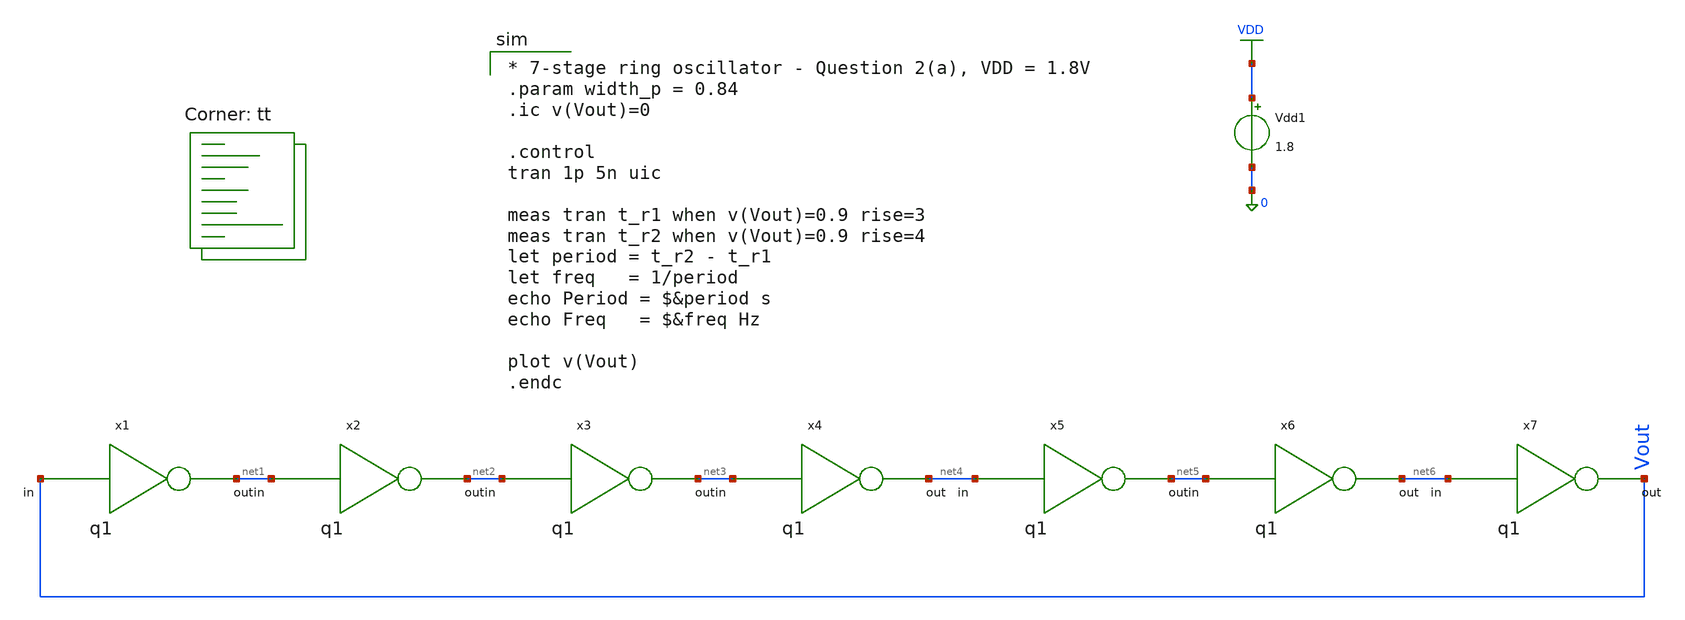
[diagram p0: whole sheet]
** sch_path: tutorial-3/source/q2a.sch
**.subckt q2a
x1 net1 Vout q1
x2 net2 net1 q1
x3 net3 net2 q1
x4 net4 net3 q1
x5 net5 net4 q1
x6 net6 net5 q1
x7 Vout net6 q1
Vdd1 VDD 0 1.8
**** begin user architecture code

* 7-stage ring oscillator - Question 2(a), VDD = 1.8V
.param width_p = 0.84
.ic v(Vout)=0

.control
tran 1p 5n uic

meas tran t_r1 when v(Vout)=0.9 rise=3
meas tran t_r2 when v(Vout)=0.9 rise=4
let period = t_r2 - t_r1
let freq   = 1/period
echo Period = $&period s
echo Freq   = $&freq Hz

plot v(Vout)
.endc

.lib $::SKYWATER_MODELS/sky130.lib.spice tt
**** end user architecture code
**.ends

* expanding   symbol:  q1.sym # of pins=2
** sym_path: tutorial-3/source/q1.sym
** sch_path: tutorial-3/source/q1.sch
.subckt q1 out in
*.ipin in
*.opin out
XM1 out in VDD VDD sky130_fd_pr__pfet_01v8 L=0.15 W={width_p} nf=1 ad='int((nf+1)/2) * W/nf * 0.29' as='int((nf+2)/2) * W/nf * 0.29'
+ pd='2*int((nf+1)/2) * (W/nf + 0.29)' ps='2*int((nf+2)/2) * (W/nf + 0.29)' nrd='0.29 / W' nrs='0.29 / W'
+ sa=0 sb=0 sd=0 mult=1 m=1
XM2 out in GND GND sky130_fd_pr__nfet_01v8 L=0.15 W=0.42 nf=1 ad='int((nf+1)/2) * W/nf * 0.29' as='int((nf+2)/2) * W/nf * 0.29'
+ pd='2*int((nf+1)/2) * (W/nf + 0.29)' ps='2*int((nf+2)/2) * (W/nf + 0.29)' nrd='0.29 / W' nrs='0.29 / W'
+ sa=0 sb=0 sd=0 mult=1 m=1
.ends

.GLOBAL VDD
.GLOBAL GND
.end
